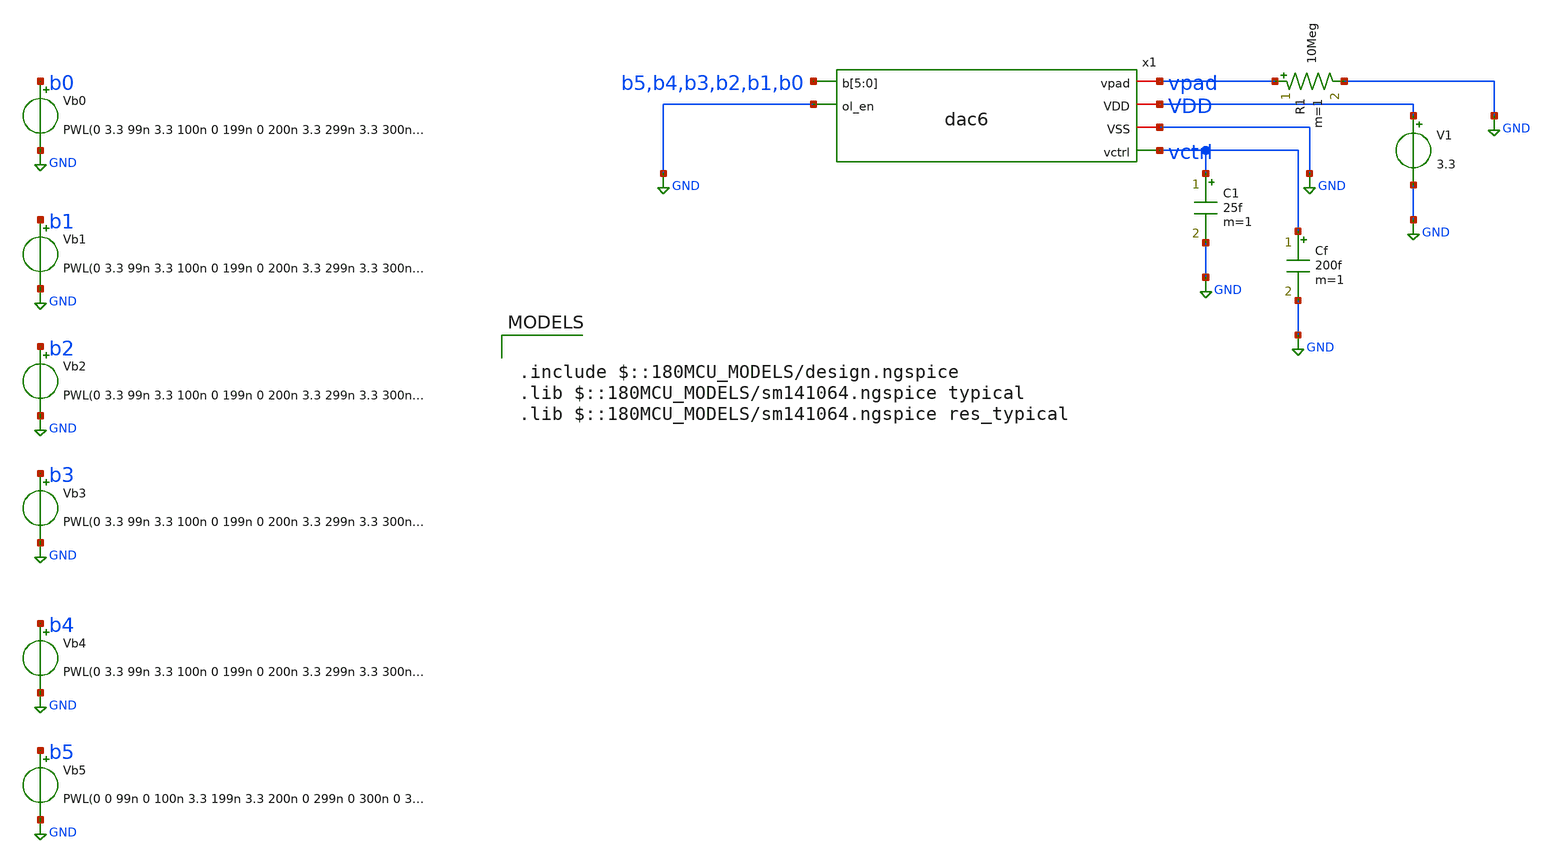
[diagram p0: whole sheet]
** sch_path: xschem/pll_dac/tb_dac6_settle.sch
**.subckt tb_dac6_settle
x1 b5 b4 b3 b2 b1 b0 GND vpad VDD GND vctrl dac6
V1 VDD GND 3.3
C1 vctrl GND 25f m=1
R1 vpad GND 10Meg m=1
Vb0 b0 GND PWL(0 3.3 99n 3.3 100n 0 199n 0 200n 3.3 299n 3.3 300n 3.3 399n 3.3 400n 0 499n 0 500n
+ 3.3 599n 3.3 600n 0 699n 0 700n 0 799n 0 800n 3.3 899n 3.3 900n 0 999n 0)
Vb2 b2 GND PWL(0 3.3 99n 3.3 100n 0 199n 0 200n 3.3 299n 3.3 300n 3.3 399n 3.3 400n 0 499n 0 500n
+ 3.3 599n 3.3 600n 0 699n 0 700n 0 799n 0 800n 3.3 899n 3.3 900n 0 999n 0)
Vb1 b1 GND PWL(0 3.3 99n 3.3 100n 0 199n 0 200n 3.3 299n 3.3 300n 3.3 399n 3.3 400n 0 499n 0 500n
+ 3.3 599n 3.3 600n 0 699n 0 700n 0 799n 0 800n 3.3 899n 3.3 900n 0 999n 0)
Vb3 b3 GND PWL(0 3.3 99n 3.3 100n 0 199n 0 200n 3.3 299n 3.3 300n 3.3 399n 3.3 400n 0 499n 0 500n
+ 3.3 599n 3.3 600n 0 699n 0 700n 0 799n 0 800n 3.3 899n 3.3 900n 0 999n 0)
Vb4 b4 GND PWL(0 3.3 99n 3.3 100n 0 199n 0 200n 3.3 299n 3.3 300n 0 399n 0 400n 3.3 499n 3.3 500n 0
+ 599n 0 600n 3.3 699n 3.3 700n 0 799n 0 800n 3.3 899n 3.3 900n 0 999n 0)
Vb5 b5 GND PWL(0 0 99n 0 100n 3.3 199n 3.3 200n 0 299n 0 300n 0 399n 0 400n 0 499n 0 500n 3.3 599n
+ 3.3 600n 3.3 699n 3.3 700n 0 799n 0 800n 3.3 899n 3.3 900n 0 999n 0)
Cf vctrl GND 200f m=1
**** begin user architecture code

.include $::180MCU_MODELS/design.ngspice
.lib $::180MCU_MODELS/sm141064.ngspice typical
.lib $::180MCU_MODELS/sm141064.ngspice res_typical



.control
save v(vctrl)
tran 0.1n 1u
linearize v(vctrl)
let vv = v(vctrl)
let codes = vector(10)
let codes[0]=31
let codes[1]=32
let codes[2]=31
let codes[3]=15
let codes[4]=16
let codes[5]=47
let codes[6]=48
let codes[7]=0
let codes[8]=63
let codes[9]=0
let tol = 0.5 * 0.0309
let e = 1
while e < 10
  let i0 = e*1000
  let i1 = e*1000 + 950
  let vstart = vv[i0-10]
  let vfinal = vv[i1]
  let w = vv[i0,i1]
  let hi = vecmax(w)
  let lo = vecmin(w)
  let top = vfinal
  let bot = vstart
  if vstart > vfinal
    let top = vstart
    let bot = vfinal
  end
  let glitch = 0
  if hi - top > glitch
    let glitch = hi - top
  end
  if bot - lo > glitch
    let glitch = bot - lo
  end
  let k = i1
  let last = i0
  while k >= i0
    if abs(vv[k] - vfinal) > tol
      let last = k
      let k = i0 - 1
    end
    let k = k - 1
  end
  let tset = (last - i0) * 0.1
  let cfrom = codes[e-1]
  let cto = codes[e]
  echo $&cfrom to $&cto :  settle $&tset ns   glitch $&glitch V   final $&vfinal V
  let e = e + 1
end
plot v(vctrl) title 'VCTRL during fast code changes'
.endc


**** end user architecture code
**.ends

* expanding   symbol:  pll_dac/dac6.sym # of pins=6
** sym_path: xschem/pll_dac/dac6.sym
** sch_path: xschem/pll_dac/dac6.sch
.subckt dac6 b[5] b[4] b[3] b[2] b[1] b[0] ol_en vpad VDD VSS vctrl
*.ipin b[5],b[4],b[3],b[2],b[1],b[0]
*.ipin ol_en
*.iopin vpad
*.iopin VDD
*.iopin VSS
*.opin vctrl
x1 VDD b[5] b[4] b[3] b[2] b[1] b[0] VSS vctrl schr2r6
XRD1 rd vctrl VSS ppolyf_u_1k r_width=1u r_length=61u m=1
XRD2[1] VSS rd VSS ppolyf_u_1k r_width=1u r_length=61u m=1
XRD2[0] VSS rd VSS ppolyf_u_1k r_width=1u r_length=61u m=1
XOL VDD ol_en ol_en_b VSS sw_inv
XM2 vctrl ol_en_b vpad VDD pfet_03v3 L=0.28u W=5.6u nf=1 ad='int((nf+1)/2) * W/nf * 0.18u' as='int((nf+2)/2) * W/nf * 0.18u'
+ pd='2*int((nf+1)/2) * (W/nf + 0.18u)' ps='2*int((nf+2)/2) * (W/nf + 0.18u)' nrd='0.18u / W' nrs='0.18u / W'
+ sa=0 sb=0 sd=0 m=1
XM1 vctrl ol_en vpad VSS nfet_03v3 L=0.28u W=2u nf=1 ad='int((nf+1)/2) * W/nf * 0.18u' as='int((nf+2)/2) * W/nf * 0.18u'
+ pd='2*int((nf+1)/2) * (W/nf + 0.18u)' ps='2*int((nf+2)/2) * (W/nf + 0.18u)' nrd='0.18u / W' nrs='0.18u / W'
+ sa=0 sb=0 sd=0 m=1
.ends


* expanding   symbol:  pll_dac/schr2r6.sym # of pins=4
** sym_path: xschem/pll_dac/schr2r6.sym
** sch_path: xschem/pll_dac/schr2r6.sch
.subckt schr2r6 VDD b[5] b[4] b[3] b[2] b[1] b[0] VSS lad
*.iopin VDD
*.iopin VSS
*.ipin b[5],b[4],b[3],b[2],b[1],b[0]
*.opin lad
XI[5] VDD b[5] d[5] VSS sw_inv
XI[4] VDD b[4] d[4] VSS sw_inv
XI[3] VDD b[3] d[3] VSS sw_inv
XI[2] VDD b[2] d[2] VSS sw_inv
XI[1] VDD b[1] d[1] VSS sw_inv
XI[0] VDD b[0] d[0] VSS sw_inv
XIT VDD VDD dt VSS sw_inv
XRLa[5] m[5] d[5] VSS ppolyf_u_1k r_width=1u r_length=61u m=1
XRLa[4] m[4] d[4] VSS ppolyf_u_1k r_width=1u r_length=61u m=1
XRLa[3] m[3] d[3] VSS ppolyf_u_1k r_width=1u r_length=61u m=1
XRLa[2] m[2] d[2] VSS ppolyf_u_1k r_width=1u r_length=61u m=1
XRLa[1] m[1] d[1] VSS ppolyf_u_1k r_width=1u r_length=61u m=1
XRLa[0] m[0] d[0] VSS ppolyf_u_1k r_width=1u r_length=61u m=1
XRLb[5] lad m[5] VSS ppolyf_u_1k r_width=1u r_length=61u m=1
XRLb[4] j[4] m[4] VSS ppolyf_u_1k r_width=1u r_length=61u m=1
XRLb[3] j[3] m[3] VSS ppolyf_u_1k r_width=1u r_length=61u m=1
XRLb[2] j[2] m[2] VSS ppolyf_u_1k r_width=1u r_length=61u m=1
XRLb[1] j[1] m[1] VSS ppolyf_u_1k r_width=1u r_length=61u m=1
XRLb[0] j[0] m[0] VSS ppolyf_u_1k r_width=1u r_length=61u m=1
XRR[4] lad j[4] VSS ppolyf_u_1k r_width=1u r_length=61u m=1
XRR[3] j[4] j[3] VSS ppolyf_u_1k r_width=1u r_length=61u m=1
XRR[2] j[3] j[2] VSS ppolyf_u_1k r_width=1u r_length=61u m=1
XRR[1] j[2] j[1] VSS ppolyf_u_1k r_width=1u r_length=61u m=1
XRR[0] j[1] j[0] VSS ppolyf_u_1k r_width=1u r_length=61u m=1
XRTa mt dt VSS ppolyf_u_1k r_width=1u r_length=61u m=1
XRTb j[0] mt VSS ppolyf_u_1k r_width=1u r_length=61u m=1
XRDUM[3] VSS VSS VSS ppolyf_u_1k r_width=1u r_length=61u m=1
XRDUM[2] VSS VSS VSS ppolyf_u_1k r_width=1u r_length=61u m=1
XRDUM[1] VSS VSS VSS ppolyf_u_1k r_width=1u r_length=61u m=1
XRDUM[0] VSS VSS VSS ppolyf_u_1k r_width=1u r_length=61u m=1
.ends


* expanding   symbol:  pll_dac/sw_inv.sym # of pins=4
** sym_path: xschem/pll_dac/sw_inv.sym
** sch_path: xschem/pll_dac/sw_inv.sch
.subckt sw_inv VDD A Y VSS
*.ipin A
*.iopin VDD
*.iopin VSS
*.opin Y
XM1 Y A VSS VSS nfet_03v3 L=0.28u W=2u nf=1 ad='int((nf+1)/2) * W/nf * 0.18u' as='int((nf+2)/2) * W/nf * 0.18u'
+ pd='2*int((nf+1)/2) * (W/nf + 0.18u)' ps='2*int((nf+2)/2) * (W/nf + 0.18u)' nrd='0.18u / W' nrs='0.18u / W'
+ sa=0 sb=0 sd=0 m=1
XM2 Y A VDD VDD pfet_03v3 L=0.28u W=5.6u nf=1 ad='int((nf+1)/2) * W/nf * 0.18u' as='int((nf+2)/2) * W/nf * 0.18u'
+ pd='2*int((nf+1)/2) * (W/nf + 0.18u)' ps='2*int((nf+2)/2) * (W/nf + 0.18u)' nrd='0.18u / W' nrs='0.18u / W'
+ sa=0 sb=0 sd=0 m=1
.ends

.GLOBAL GND
.end
